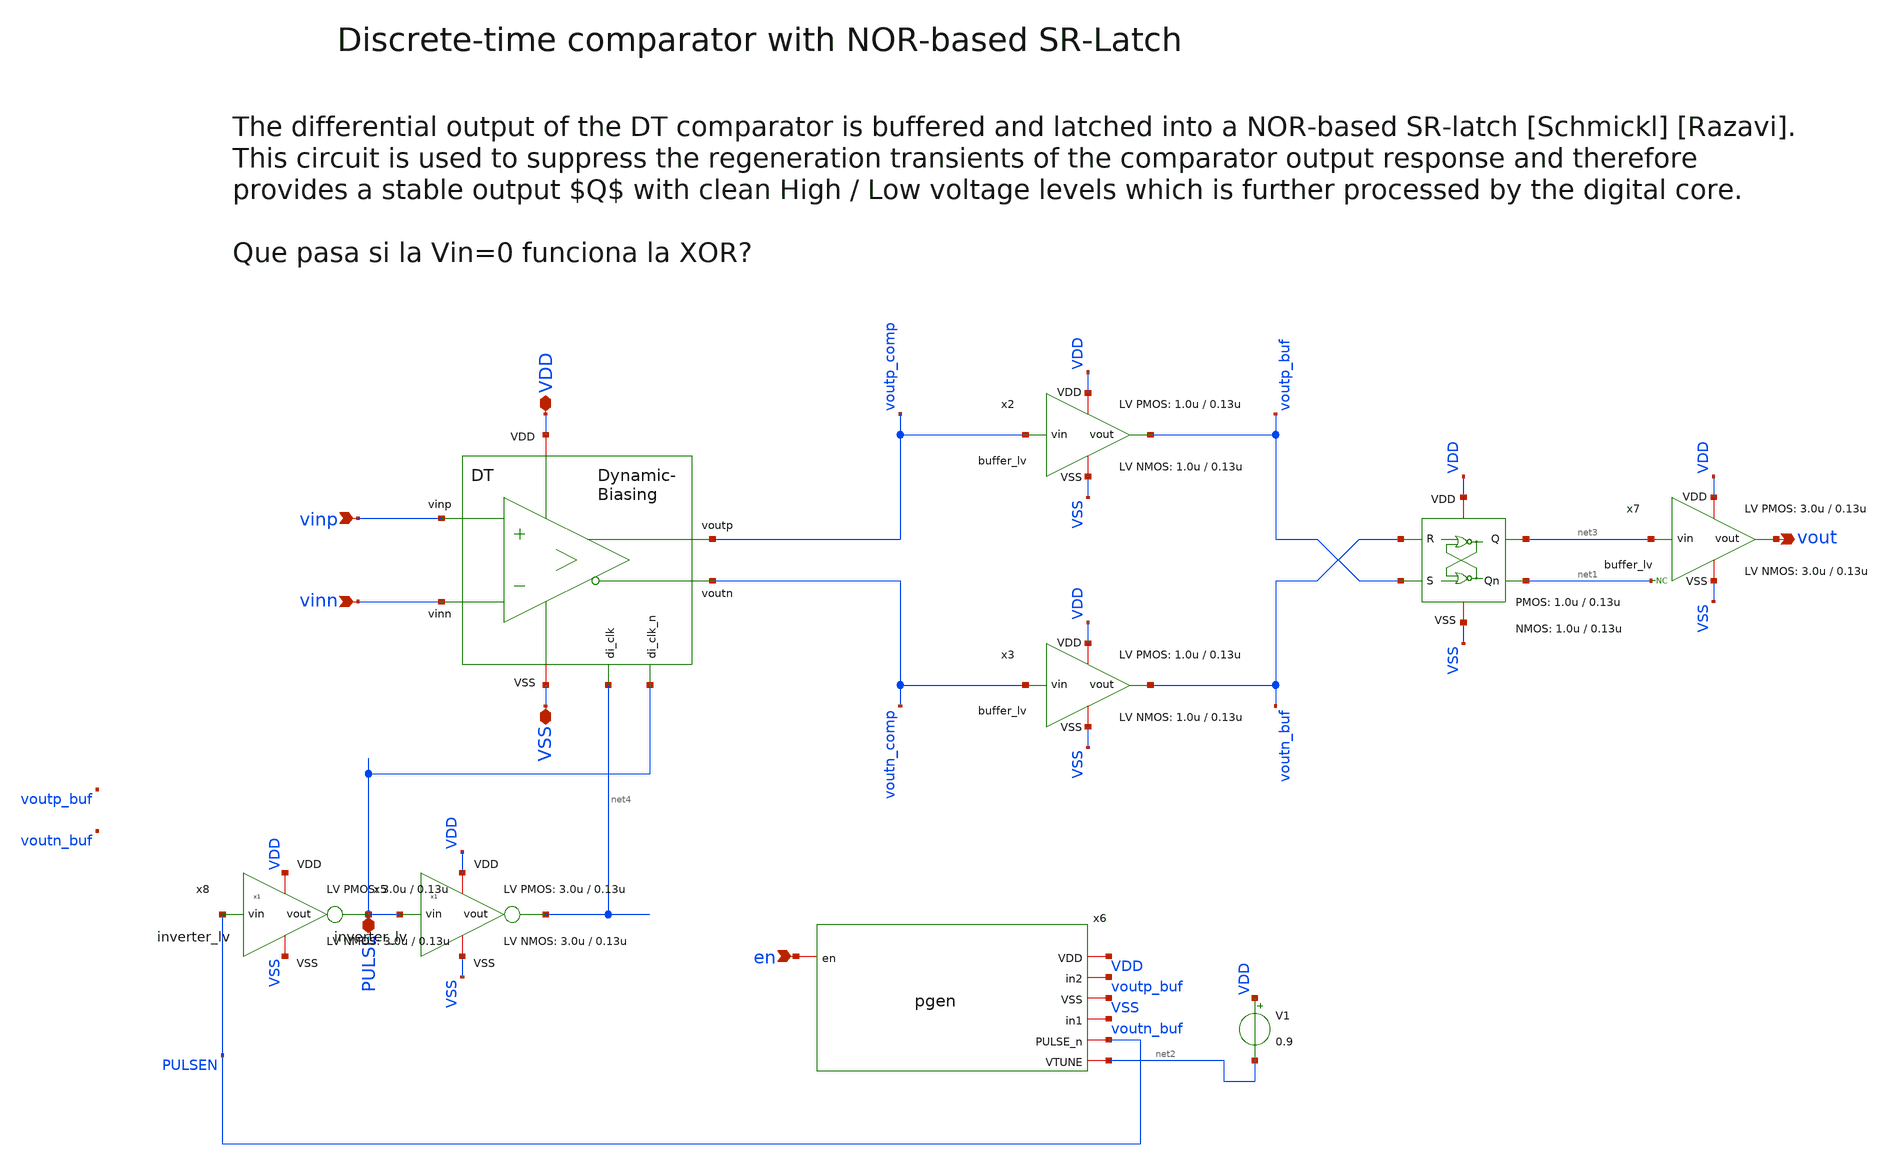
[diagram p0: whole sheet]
** sch_path: xschem/comparator/discrete_time/DT_comparator.sch
**.subckt DT_comparator VDD vout VSS vinp vinn en PULSE
*.iopin VDD
*.opin vout
*.iopin VSS
*.ipin vinp
*.ipin vinn
*.ipin en
*.iopin PULSE
x2 VDD voutp_comp voutp_buf VSS buffer_lv W_P_INV=1.0u L_P_INV=0.13u W_N_INV=1.0u L_N_INV=0.13u
x3 VDD voutn_comp voutn_buf VSS buffer_lv W_P_INV=1.0u L_P_INV=0.13u W_N_INV=1.0u L_N_INV=0.13u
x5 VDD PULSE net4 VSS inverter_lv W_P=3.0u L_P=0.13u W_N=3.0u L_N=0.13u N_C=1
* noconn #net1
x4 VDD voutp_buf net1 VSS net3 voutn_buf SR_latch W_P_SR=1.0u L_P_SR=0.13u W_N_SR=1.0u L_N_SR=0.13u
x6 VDD voutp_buf VSS voutn_buf PULSEN net2 en pgen
V1 VDD net2 0.9
x1 PULSE net4 VDD voutp_comp vinp VSS voutn_comp vinn dynamic_biasing_comparator
x7 VDD net3 vout VSS buffer_lv W_P_INV=3.0u L_P_INV=0.13u W_N_INV=3.0u L_N_INV=0.13u
x8 VDD PULSEN PULSE VSS inverter_lv W_P=3.0u L_P=0.13u W_N=3.0u L_N=0.13u N_C=1
**.ends
.end
